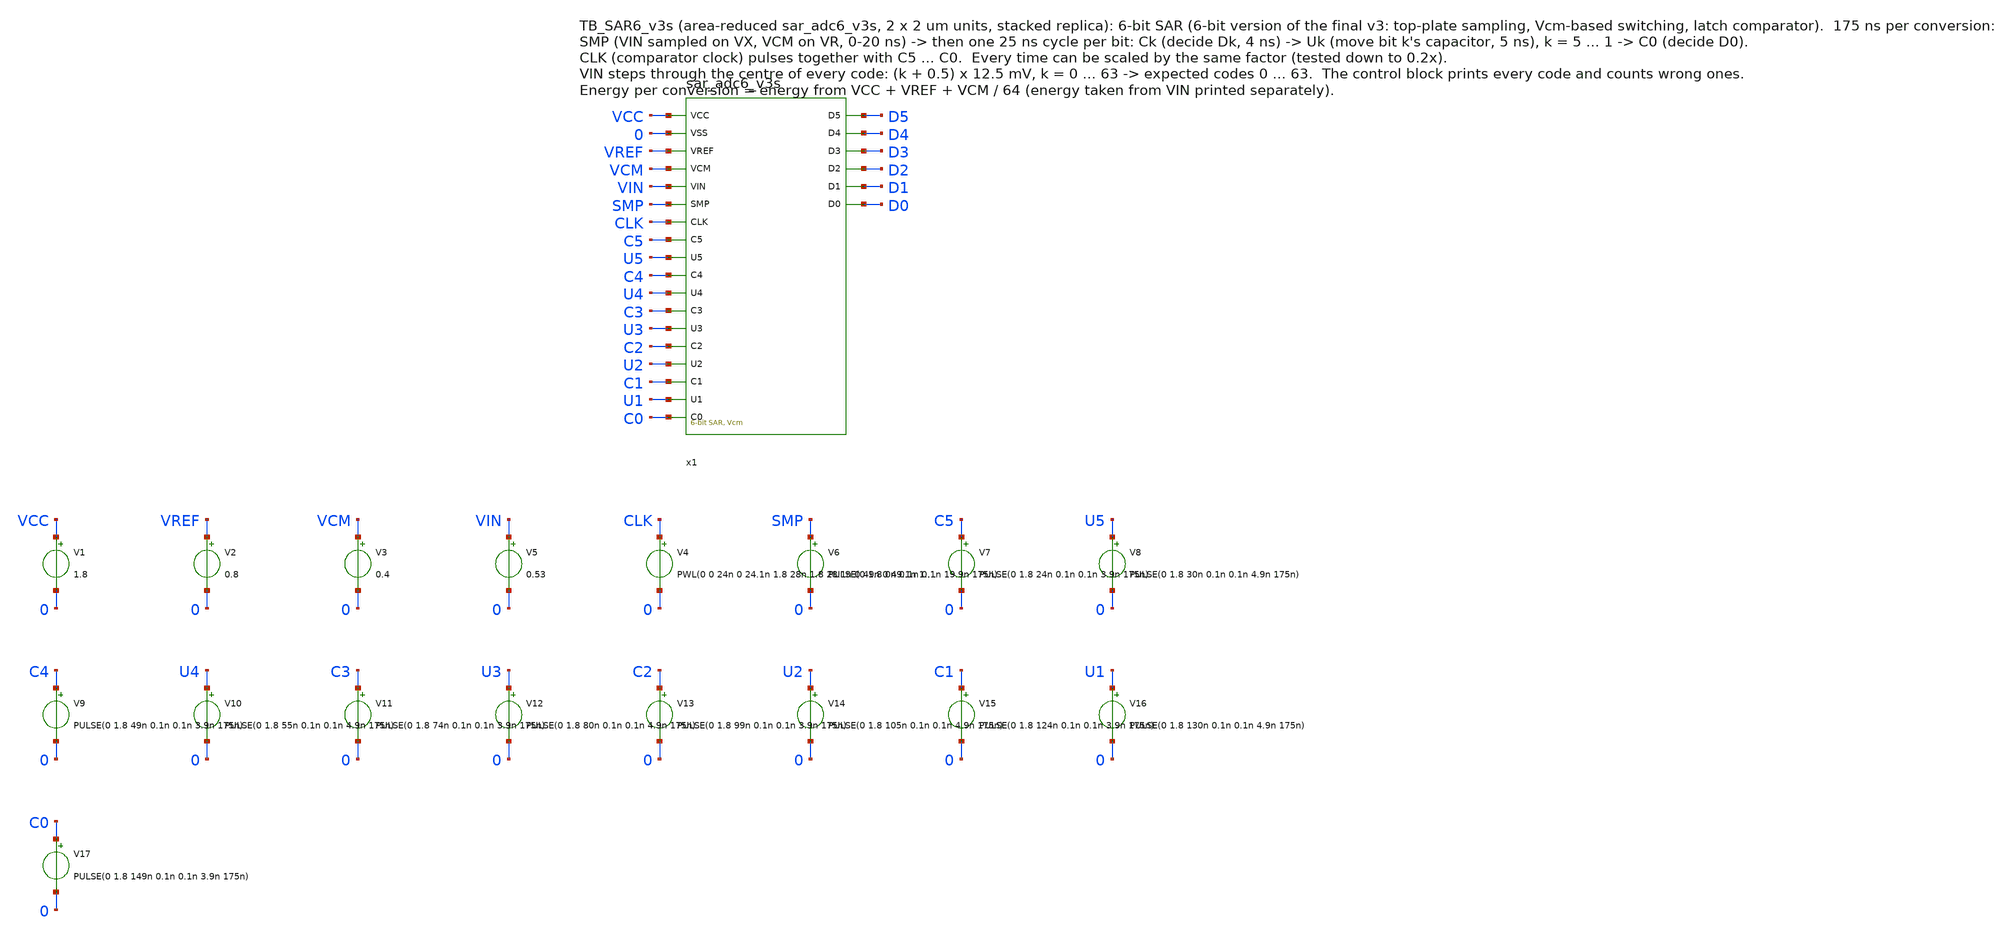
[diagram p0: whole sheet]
** sch_path: SAR_improved/TB_SAR6_v3s.sch
**.subckt TB_SAR6_v3s
x1 VCC 0 VREF VCM VIN SMP CLK C5 U5 C4 U4 C3 U3 C2 U2 C1 U1 C0 D5 D4 D3 D2 D1 D0 sar_adc6_v3s
V1 VCC 0 1.8
V2 VREF 0 0.8
V3 VCM 0 0.4
V5 VIN 0 0.53
V4 CLK 0 PWL(0 0 24n 0 24.1n 1.8 28n 1.8 28.1n 0 49n 0 49.1n 1.8 53n 1.8 53.1n 0 74n 0 74.1n 1.8 78n
+ 1.8 78.1n 0 99n 0 99.1n 1.8 103n 1.8 103.1n 0 124n 0 124.1n 1.8 128n 1.8 128.1n 0 149n 0 149.1n 1.8
+ 153n 1.8 153.1n 0 175n 0) r=0
V6 SMP 0 PULSE(0 1.8 0n 0.1n 0.1n 19.9n 175n)
V7 C5 0 PULSE(0 1.8 24n 0.1n 0.1n 3.9n 175n)
V8 U5 0 PULSE(0 1.8 30n 0.1n 0.1n 4.9n 175n)
V9 C4 0 PULSE(0 1.8 49n 0.1n 0.1n 3.9n 175n)
V10 U4 0 PULSE(0 1.8 55n 0.1n 0.1n 4.9n 175n)
V11 C3 0 PULSE(0 1.8 74n 0.1n 0.1n 3.9n 175n)
V12 U3 0 PULSE(0 1.8 80n 0.1n 0.1n 4.9n 175n)
V13 C2 0 PULSE(0 1.8 99n 0.1n 0.1n 3.9n 175n)
V14 U2 0 PULSE(0 1.8 105n 0.1n 0.1n 4.9n 175n)
V15 C1 0 PULSE(0 1.8 124n 0.1n 0.1n 3.9n 175n)
V16 U1 0 PULSE(0 1.8 130n 0.1n 0.1n 4.9n 175n)
V17 C0 0 PULSE(0 1.8 149n 0.1n 0.1n 3.9n 175n)
**** begin user architecture code

.lib /home/ttuser/pdk/sky130A/libs.tech/combined/sky130.lib.spice tt
.option method=gear reltol=1e-4
.control
save all
tran 0.05n 11200n
let code = 0*v(D0)
let code = code + 32*ceil((v(D5)-0.9)/10)
let code = code + 16*ceil((v(D4)-0.9)/10)
let code = code + 8*ceil((v(D3)-0.9)/10)
let code = code + 4*ceil((v(D2)-0.9)/10)
let code = code + 2*ceil((v(D1)-0.9)/10)
let code = code + 1*ceil((v(D0)-0.9)/10)
let nwrong = 0
let k = 0
while k < 64
  let tr = k*175e-9 + 165e-9
  meas tran ck find code at=$&tr
  print k ck
  if abs(ck - k) > 0.5
    let nwrong = nwrong + 1
  end
  let k = k + 1
end
print nwrong
let ptot = 1.8*(-i(V1)) + 0.8*(-i(V2)) + 0.4*(-i(V3))
let pin = v(VIN)*(-i(V5))
meas tran etot integ ptot from=0 to=11200n
meas tran ein integ pin from=0 to=11200n
let e_conv_pJ = etot/64*1e12
let e_from_vin_pJ = ein/64*1e12
let p_uW = etot/11200e-9*1e6
print e_conv_pJ p_uW e_from_vin_pJ
plot v(VIN) v(x1.VX) v(x1.VR)
plot v(SMP) v(CLK)+2 v(x1.COM)+4
plot v(x1.x2.BP5) v(x1.x2.BP4) v(x1.x2.BP3) v(x1.x2.BP2) v(x1.x2.BP1)
plot v(D5)+0 v(D4)+2 v(D3)+4 v(D2)+6 v(D1)+8 v(D0)+10
plot code
.endc

**** end user architecture code
**.ends
.end
